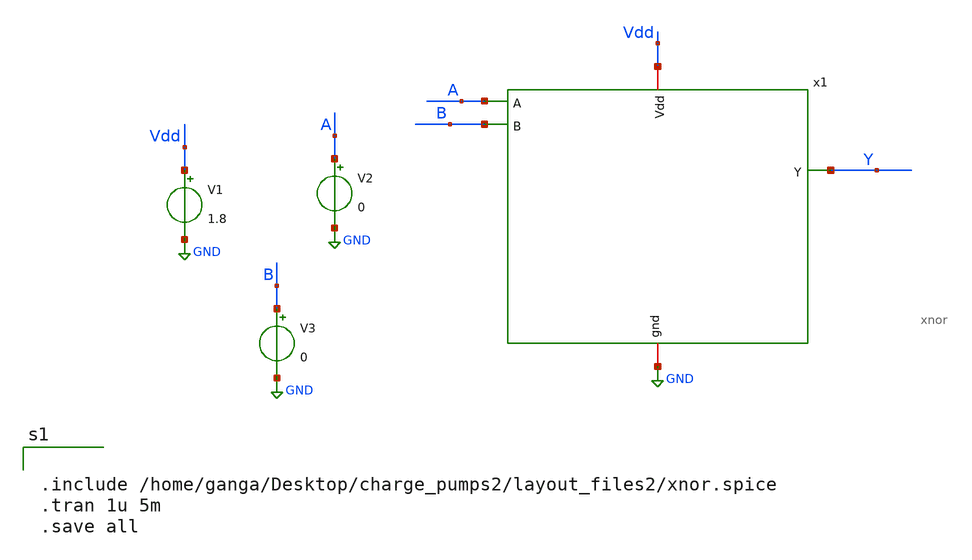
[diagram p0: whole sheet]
** sch_path: xschem/xschemfiles/xnor_tb.sch
**.subckt xnor_tb
x1 B A GND Vdd Y xnor
V2 A GND 0
V1 Vdd GND 1.8
V3 B GND 0
**** begin user architecture code


.include /home/ganga/Desktop/charge_pumps2/layout_files2/xnor.spice
.tran 1u 5m
.save all



** opencircuitdesign pdks install
.lib $::SKYWATER_MODELS/sky130.lib.spice tt


**** end user architecture code
**.ends
.GLOBAL GND
.end
